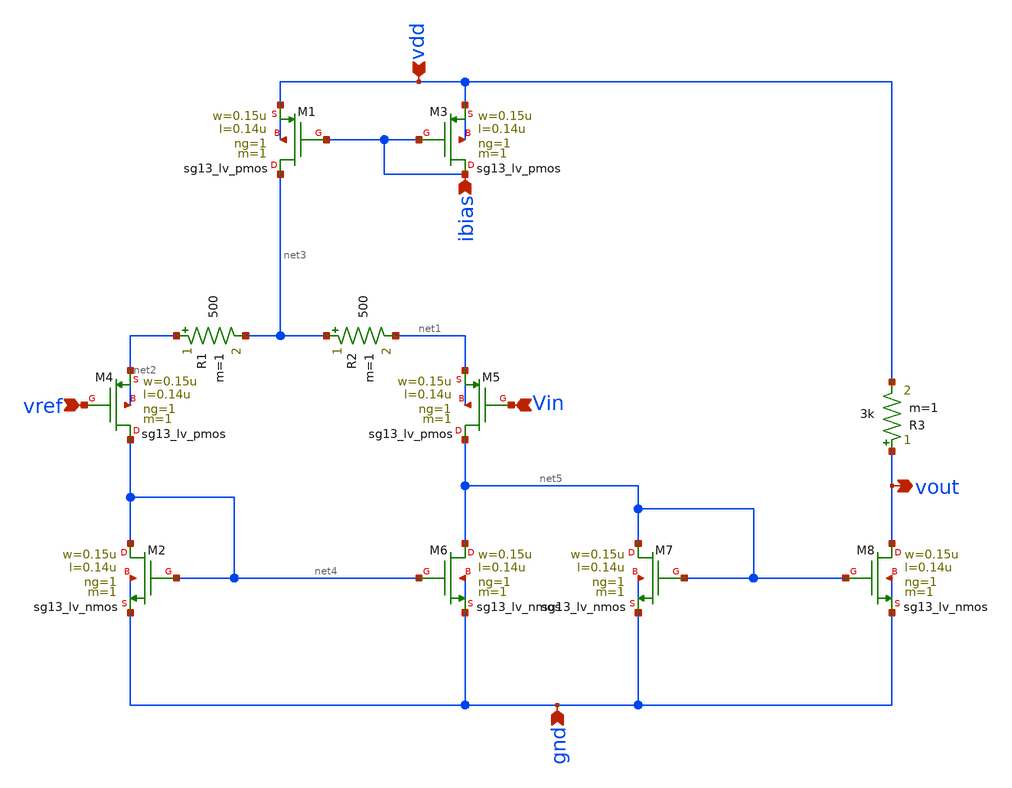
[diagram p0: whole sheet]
** sch_path: spice/decoderCell.sch
**.subckt decoderCell vdd gnd vout ibias Vin vref
*.ipin vdd
*.ipin gnd
*.opin vout
*.ipin ibias
*.ipin Vin
*.ipin vref
XM1 net3 ibias vdd vdd sg13_lv_pmos w=0.15u l=0.14u ng=1 m=1 mm_ok=1
XM2 net4 net4 gnd gnd sg13_lv_nmos w=0.15u l=0.14u ng=1 m=1 mm_ok=1
XM3 ibias ibias vdd vdd sg13_lv_pmos w=0.15u l=0.14u ng=1 m=1 mm_ok=1
XM4 net4 vref net2 net2 sg13_lv_pmos w=0.15u l=0.14u ng=1 m=1 mm_ok=1
XM5 net5 Vin net1 net1 sg13_lv_pmos w=0.15u l=0.14u ng=1 m=1 mm_ok=1
R1 net2 net3 500 m=1
R2 net3 net1 500 m=1
XM6 net5 net4 gnd gnd sg13_lv_nmos w=0.15u l=0.14u ng=1 m=1 mm_ok=1
XM7 net5 net5 gnd gnd sg13_lv_nmos w=0.15u l=0.14u ng=1 m=1 mm_ok=1
XM8 vout net5 gnd gnd sg13_lv_nmos w=0.15u l=0.14u ng=1 m=1 mm_ok=1
R3 vout vdd 3k m=1
**.ends
.end
